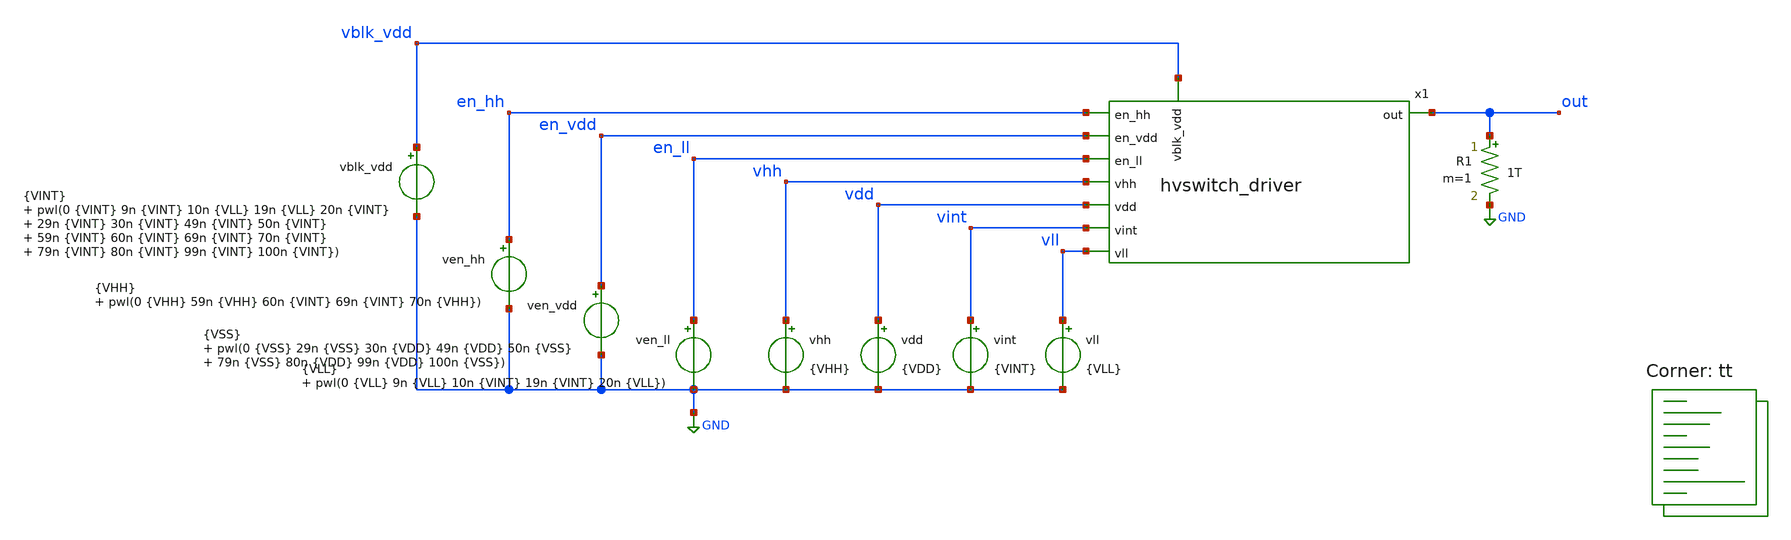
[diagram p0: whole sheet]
** sch_path: test-hvswitch_driver.sch
**.subckt test-hvswitch_driver
x1 vhh vdd en_vdd en_hh out vint en_ll vll vblk_vdd hvswitch_driver
vhh vhh GND {VHH}
vint vint GND {VINT}
vll vll GND {VLL}
ven_ll en_ll GND {VLL} pwl(0 {VLL} 9n {VLL} 10n {VINT} 19n {VINT} 20n {VLL})
vdd vdd GND {VDD}
ven_hh en_hh GND {VHH} pwl(0 {VHH} 59n {VHH} 60n {VINT} 69n {VINT} 70n {VHH})
ven_vdd en_vdd GND {VSS} pwl(0 {VSS} 29n {VSS} 30n {VDD} 49n {VDD} 50n {VSS} 79n {VSS} 80n {VDD} 99n
+ {VDD} 100n {VSS})
R1 out GND 1T m=1
vblk_vdd vblk_vdd GND {VINT} pwl(0 {VINT} 9n {VINT} 10n {VLL} 19n {VLL} 20n {VINT} 29n {VINT} 30n {VINT}
+ 49n {VINT} 50n {VINT} 59n {VINT} 60n {VINT} 69n {VINT} 70n {VINT} 79n {VINT} 80n {VINT} 99n {VINT} 100n
+ {VINT})
**** begin user architecture code
.lib $::SKYWATER_MODELS/sky130.lib.spice tt



.param VLL=-3.8
.param VDD=1.8
.param VSS=0
.param VLH=0
.param VHH=6.7
.param VINT={(VHH+VLL)/2}
.option savecurrents
.control
  save all
  op
  remzerovec
  write test-hvswitch_driver.raw
  set appendwrite
  tran 10p 120n
  remzerovec
  write test-hvswitch_driver.raw
.endc



**** end user architecture code
**.ends

* expanding   symbol:  hvswitch_driver.sym # of pins=9
** sym_path: hvswitch_driver.sym
** sch_path: hvswitch_driver.sch
.subckt hvswitch_driver vhh vdd en_vdd en_hh out vint en_ll vll vblk_vdd
*.ipin vhh
*.ipin vll
*.ipin vint
*.ipin en_hh
*.ipin en_ll
*.opin out
*.ipin vdd
*.ipin en_vdd
*.ipin vblk_vdd
XM3 llint en_ll vll vll sky130_fd_pr__nfet_g5v0d10v5 L=0.5 W=1 nf=1 ad='int((nf+1)/2) * W/nf * 0.29'
+ as='int((nf+2)/2) * W/nf * 0.29' pd='2*int((nf+1)/2) * (W/nf + 0.29)' ps='2*int((nf+2)/2) * (W/nf + 0.29)'
+ nrd='0.29 / W' nrs='0.29 / W' sa=0 sb=0 sd=0 mult=1 m=1
XM1 hhint en_hh vhh vhh sky130_fd_pr__pfet_g5v0d10v5 L=0.5 W=1 nf=1 ad='int((nf+1)/2) * W/nf * 0.29'
+ as='int((nf+2)/2) * W/nf * 0.29' pd='2*int((nf+1)/2) * (W/nf + 0.29)' ps='2*int((nf+2)/2) * (W/nf + 0.29)'
+ nrd='0.29 / W' nrs='0.29 / W' sa=0 sb=0 sd=0 mult=1 m=1
XM2 out vint hhint vhh sky130_fd_pr__pfet_g5v0d10v5 L=0.5 W=1 nf=1 ad='int((nf+1)/2) * W/nf * 0.29' as='int((nf+2)/2) * W/nf * 0.29'
+ pd='2*int((nf+1)/2) * (W/nf + 0.29)' ps='2*int((nf+2)/2) * (W/nf + 0.29)' nrd='0.29 / W' nrs='0.29 / W'
+ sa=0 sb=0 sd=0 mult=1 m=1
XM4 out vint llint vll sky130_fd_pr__nfet_g5v0d10v5 L=0.5 W=1 nf=1 ad='int((nf+1)/2) * W/nf * 0.29' as='int((nf+2)/2) * W/nf * 0.29'
+ pd='2*int((nf+1)/2) * (W/nf + 0.29)' ps='2*int((nf+2)/2) * (W/nf + 0.29)' nrd='0.29 / W' nrs='0.29 / W'
+ sa=0 sb=0 sd=0 mult=1 m=1
XM5 ddint en_vdd vdd vll sky130_fd_pr__nfet_g5v0d10v5 L=0.5 W=1 nf=1 ad='int((nf+1)/2) * W/nf * 0.29'
+ as='int((nf+2)/2) * W/nf * 0.29' pd='2*int((nf+1)/2) * (W/nf + 0.29)' ps='2*int((nf+2)/2) * (W/nf + 0.29)'
+ nrd='0.29 / W' nrs='0.29 / W' sa=0 sb=0 sd=0 mult=1 m=1
XM6 out vblk_vdd ddint vll sky130_fd_pr__nfet_g5v0d10v5 L=0.5 W=1 nf=1 ad='int((nf+1)/2) * W/nf * 0.29'
+ as='int((nf+2)/2) * W/nf * 0.29' pd='2*int((nf+1)/2) * (W/nf + 0.29)' ps='2*int((nf+2)/2) * (W/nf + 0.29)'
+ nrd='0.29 / W' nrs='0.29 / W' sa=0 sb=0 sd=0 mult=1 m=1
.ends

.GLOBAL GND
.end
